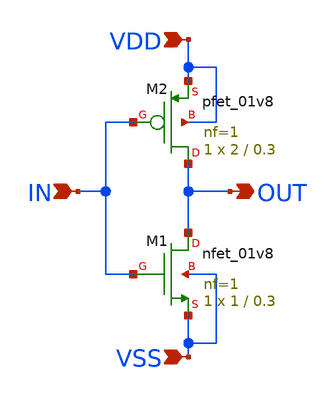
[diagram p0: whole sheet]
** sch_path: Inverter.sch
**.subckt Inverter IN VSS VDD OUT
*.ipin IN
*.ipin VSS
*.ipin VDD
*.opin OUT
XM1 OUT IN VSS VSS sky130_fd_pr__nfet_01v8 L=0.3 W=1 nf=1 ad='int((nf+1)/2) * W/nf * 0.29' as='int((nf+2)/2) * W/nf * 0.29'
+ pd='2*int((nf+1)/2) * (W/nf + 0.29)' ps='2*int((nf+2)/2) * (W/nf + 0.29)' nrd='0.29 / W' nrs='0.29 / W'
+ sa=0 sb=0 sd=0 mult=1 m=1
XM2 OUT IN VDD VDD sky130_fd_pr__pfet_01v8 L=0.3 W=2 nf=1 ad='int((nf+1)/2) * W/nf * 0.29' as='int((nf+2)/2) * W/nf * 0.29'
+ pd='2*int((nf+1)/2) * (W/nf + 0.29)' ps='2*int((nf+2)/2) * (W/nf + 0.29)' nrd='0.29 / W' nrs='0.29 / W'
+ sa=0 sb=0 sd=0 mult=1 m=1
**.ends
.end
